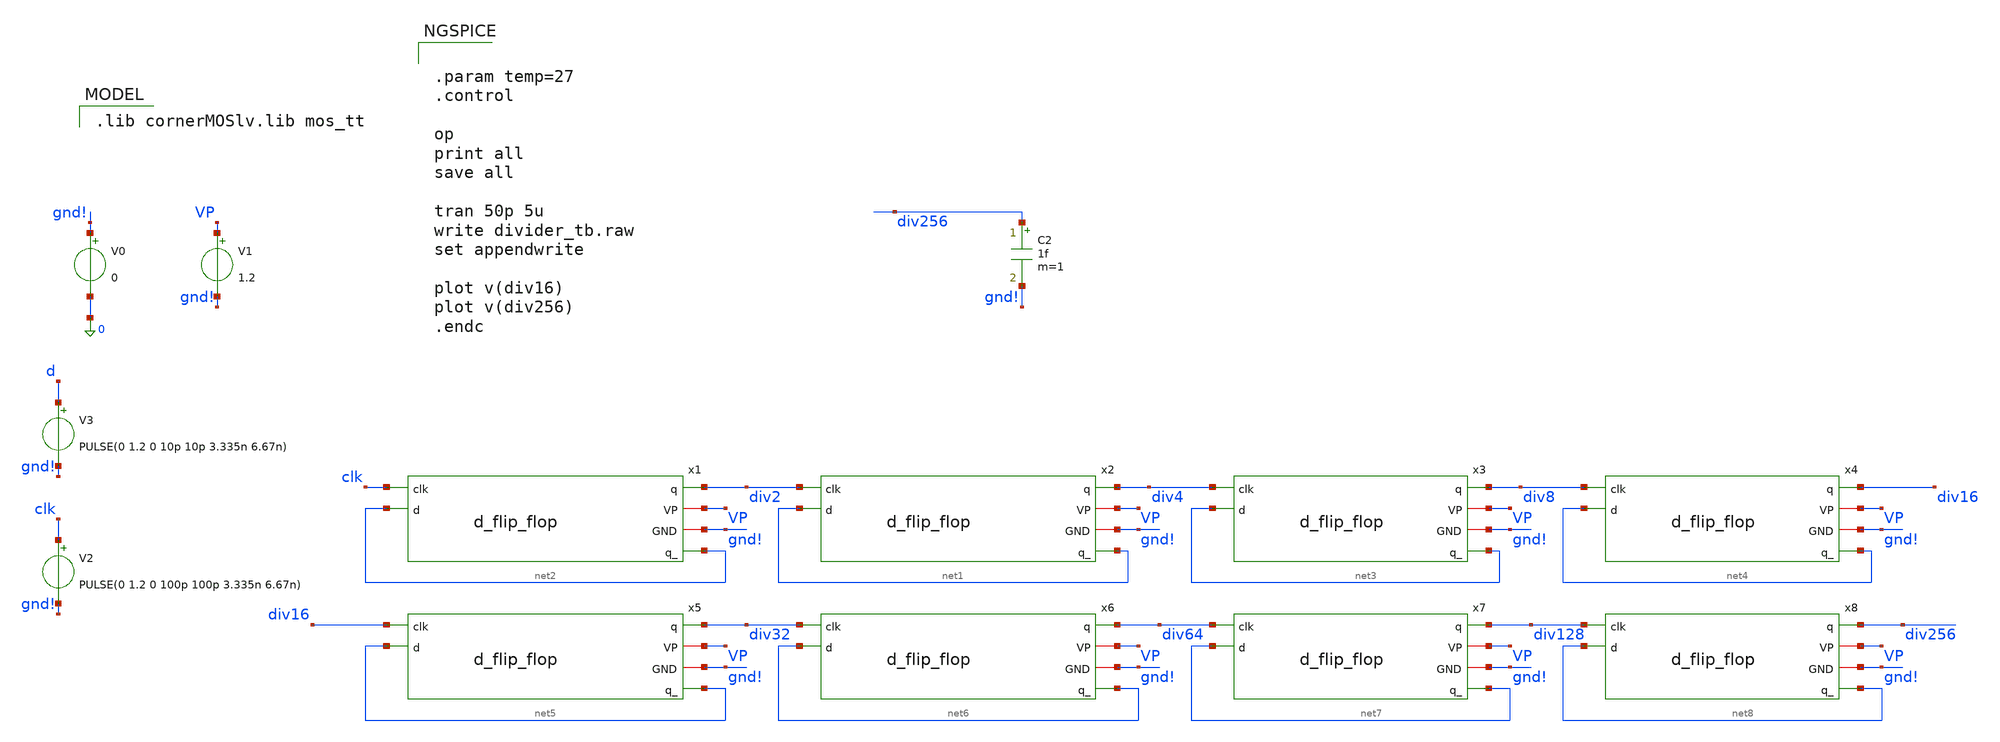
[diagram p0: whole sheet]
** sch_path: schematics/divider/divider32_tb.sch
**.subckt divider32_tb
V1 VP gnd! 1.2
V2 clk gnd! PULSE(0 1.2 0 100p 100p 3.335n 6.67n)
V0 gnd! 0 0
C2 div256 gnd! 1f m=1
x1 div2 VP gnd! net2 clk net2 d_flip_flop
x2 div4 VP gnd! net1 div2 net1 d_flip_flop
x3 div8 VP gnd! net3 div4 net3 d_flip_flop
x4 div16 VP gnd! net4 div8 net4 d_flip_flop
x5 div32 VP gnd! net5 div16 net5 d_flip_flop
V3 d gnd! PULSE(0 1.2 0 10p 10p 3.335n 6.67n)
x6 div64 VP gnd! net6 div32 net6 d_flip_flop
x7 div128 VP gnd! net7 div64 net7 d_flip_flop
x8 div256 VP gnd! net8 div128 net8 d_flip_flop
**** begin user architecture code
 .lib cornerMOSlv.lib mos_tt



.param temp=27
.control

op
print all
save all

tran 50p 5u
write divider_tb.raw
set appendwrite

plot v(div16)
plot v(div256)
.endc


**** end user architecture code
**.ends
.end
